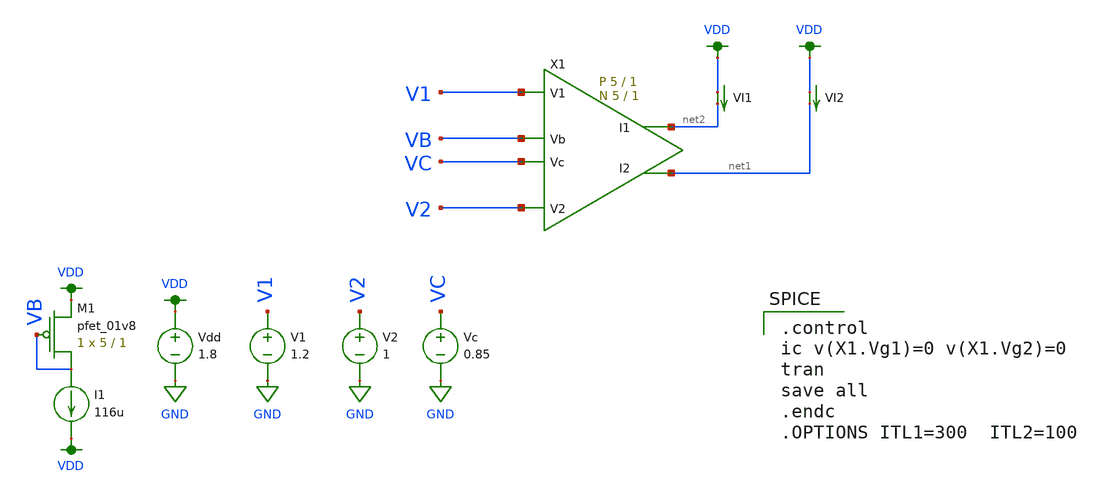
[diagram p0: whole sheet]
** sch_path: schematic/test/fgmos_diffpair_test.sch
**.subckt fgmos_diffpair_test
X1 V1 V2 net1 net2 VB VC fgmos_diffpair Wp=5 Lp=1 WW=5 LL=1
VI1 VDD net2 0
.save i(vi1)
VI2 VDD net1 0
.save i(vi2)
V1 V1 GND 1.2
V2 V2 GND 1
Vdd VDD GND 1.8
Vc VC GND 0.85
XM1 VB VB VDD VDD sky130_fd_pr__pfet_01v8 L=1 W=5 nf=1 ad='int((nf+1)/2) * W/nf * 0.29' as='int((nf+2)/2) * W/nf * 0.29'
+ pd='2*int((nf+1)/2) * (W/nf + 0.29)' ps='2*int((nf+2)/2) * (W/nf + 0.29)' nrd='0.29 / W' nrs='0.29 / W'
+ sa=0 sb=0 sd=0 mult=1 m=1
I1 VB VDD 116u
**** begin user architecture code

.option wnflag=1
.param MC_SWITCH=0.0
.lib ~/skywater/skywater-pdk/libraries/sky130_fd_pr_ngspice/latest/models/sky130.lib.spice tt


.control
ic v(X1.Vg1)=0 v(X1.Vg2)=0
tran
save all
.endc
.OPTIONS ITL1=300  ITL2=100

**** end user architecture code
**.ends

* expanding   symbol:  /home/madvlsi/Documents/MADVLSI-Final_Project/schematic/fgmos_diffpair.sym #
*+ of pins=6
** sym_path: schematic/fgmos_diffpair.sym
** sch_path: schematic/fgmos_diffpair.sch
.subckt fgmos_diffpair V1 V2 I2 I1 Vb Vc  Wp=1 Lp=0.15 WW=1 LL=0.15
*.ipin Vb
*.ipin Vc
*.iopin V1
*.iopin V2
*.iopin I1
*.iopin I2
XM1a net1 Vg1 GND GND sky130_fd_pr__nfet_01v8 L=LL W=WW nf=1 ad='int((nf+1)/2) * W/nf * 0.29' as='int((nf+2)/2) * W/nf * 0.29'
+ pd='2*int((nf+1)/2) * (W/nf + 0.29)' ps='2*int((nf+2)/2) * (W/nf + 0.29)' nrd='0.29 / W' nrs='0.29 / W'
+ sa=0 sb=0 sd=0 mult=1 m=1
XM1b net2 Vg1 GND GND sky130_fd_pr__nfet_01v8 L=LL W=WW nf=1 ad='int((nf+1)/2) * W/nf * 0.29' as='int((nf+2)/2) * W/nf * 0.29'
+ pd='2*int((nf+1)/2) * (W/nf + 0.29)' ps='2*int((nf+2)/2) * (W/nf + 0.29)' nrd='0.29 / W' nrs='0.29 / W'
+ sa=0 sb=0 sd=0 mult=1 m=1
XM1c I1 Vc net2 GND sky130_fd_pr__nfet_01v8 L=LL W=WW nf=1 ad='int((nf+1)/2) * W/nf * 0.29' as='int((nf+2)/2) * W/nf * 0.29'
+ pd='2*int((nf+1)/2) * (W/nf + 0.29)' ps='2*int((nf+2)/2) * (W/nf + 0.29)' nrd='0.29 / W' nrs='0.29 / W'
+ sa=0 sb=0 sd=0 mult=1 m=1
XM2b net3 Vg2 GND GND sky130_fd_pr__nfet_01v8 L=LL W=WW nf=1 ad='int((nf+1)/2) * W/nf * 0.29' as='int((nf+2)/2) * W/nf * 0.29'
+ pd='2*int((nf+1)/2) * (W/nf + 0.29)' ps='2*int((nf+2)/2) * (W/nf + 0.29)' nrd='0.29 / W' nrs='0.29 / W'
+ sa=0 sb=0 sd=0 mult=1 m=1
XM2a net1 Vg2 GND GND sky130_fd_pr__nfet_01v8 L=LL W=WW nf=1 ad='int((nf+1)/2) * W/nf * 0.29' as='int((nf+2)/2) * W/nf * 0.29'
+ pd='2*int((nf+1)/2) * (W/nf + 0.29)' ps='2*int((nf+2)/2) * (W/nf + 0.29)' nrd='0.29 / W' nrs='0.29 / W'
+ sa=0 sb=0 sd=0 mult=1 m=1
XM2c I2 Vc net3 GND sky130_fd_pr__nfet_01v8 L=LL W=WW nf=1 ad='int((nf+1)/2) * W/nf * 0.29' as='int((nf+2)/2) * W/nf * 0.29'
+ pd='2*int((nf+1)/2) * (W/nf + 0.29)' ps='2*int((nf+2)/2) * (W/nf + 0.29)' nrd='0.29 / W' nrs='0.29 / W'
+ sa=0 sb=0 sd=0 mult=1 m=1
XMb net1 Vb VDD VDD sky130_fd_pr__pfet_01v8 L=Lp W=Wp nf=1 ad='int((nf+1)/2) * W/nf * 0.29' as='int((nf+2)/2) * W/nf * 0.29'
+ pd='2*int((nf+1)/2) * (W/nf + 0.29)' ps='2*int((nf+2)/2) * (W/nf + 0.29)' nrd='0.29 / W' nrs='0.29 / W'
+ sa=0 sb=0 sd=0 mult=1 m=1
C2b net1 Vg2 5.3p m=1
C1a Vg1 V1 1.2p m=1
C1b Vg2 V2 1.2p m=1
C2a net1 Vg1 5.3p m=1
.ends

.GLOBAL GND
.GLOBAL VDD
.end
